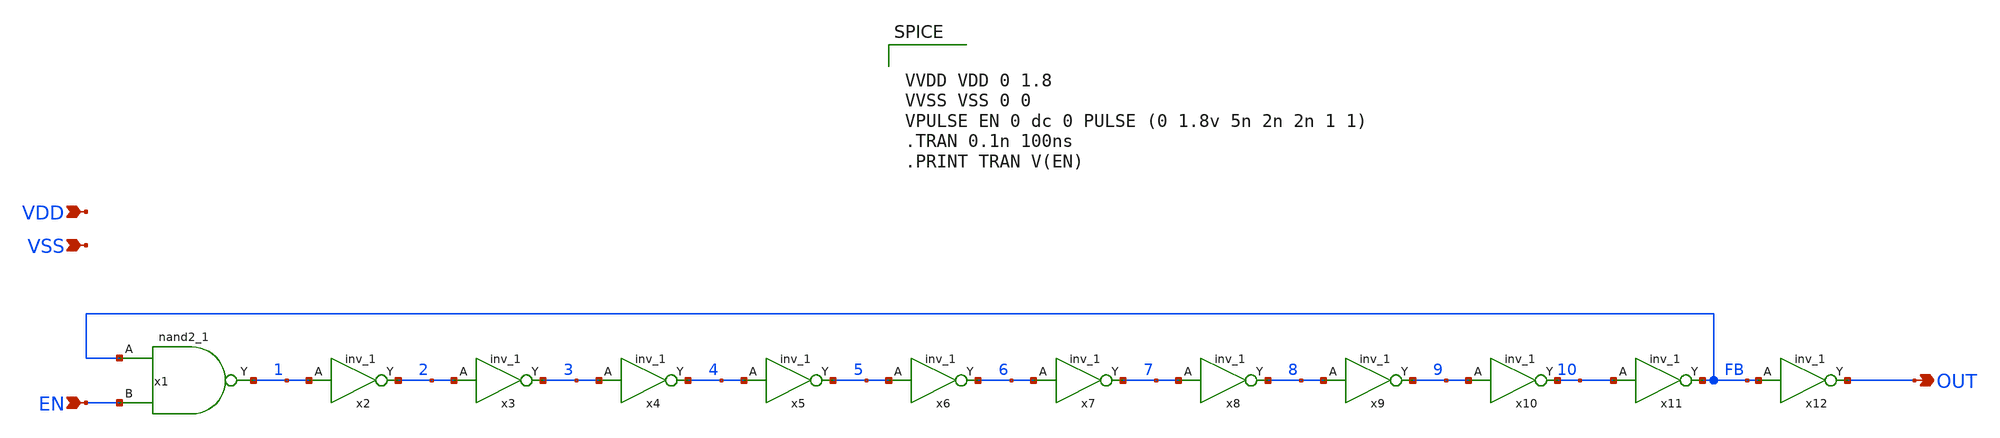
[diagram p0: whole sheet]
** sch_path: skywater/ringo.sch


VVDD VDD 0 1.8
VVSS VSS 0 0
VPULSE EN 0 dc 0 PULSE (0 1.8v 5n 2n 2n 1 1)
.TRAN 0.1n 100ns
.PRINT TRAN V(EN)



.lib $::SKYWATER_MODELS/sky130.lib.spice tt
.include $::SKYWATER_STDCELLS/sky130_fd_sc_hvl.spice

**.subckt ringo EN OUT VDD VSS
*.ipin EN
*.opin OUT
*.ipin VDD
*.ipin VSS
x1 FB EN VSS VSS VDD VDD 1 sky130_fd_sc_hvl__nand2_1
x2 1 VSS VSS VDD VDD 2 sky130_fd_sc_hvl__inv_1
x3 2 VSS VSS VDD VDD 3 sky130_fd_sc_hvl__inv_1
x4 3 VSS VSS VDD VDD 4 sky130_fd_sc_hvl__inv_1
x5 4 VSS VSS VDD VDD 5 sky130_fd_sc_hvl__inv_1
x6 5 VSS VSS VDD VDD 6 sky130_fd_sc_hvl__inv_1
x7 6 VSS VSS VDD VDD 7 sky130_fd_sc_hvl__inv_1
x8 7 VSS VSS VDD VDD 8 sky130_fd_sc_hvl__inv_1
x9 8 VSS VSS VDD VDD 9 sky130_fd_sc_hvl__inv_1
x10 9 VSS VSS VDD VDD 10 sky130_fd_sc_hvl__inv_1
x11 10 VSS VSS VDD VDD FB sky130_fd_sc_hvl__inv_1
x12 FB VSS VSS VDD VDD OUT sky130_fd_sc_hvl__inv_1
**.ends
.end
